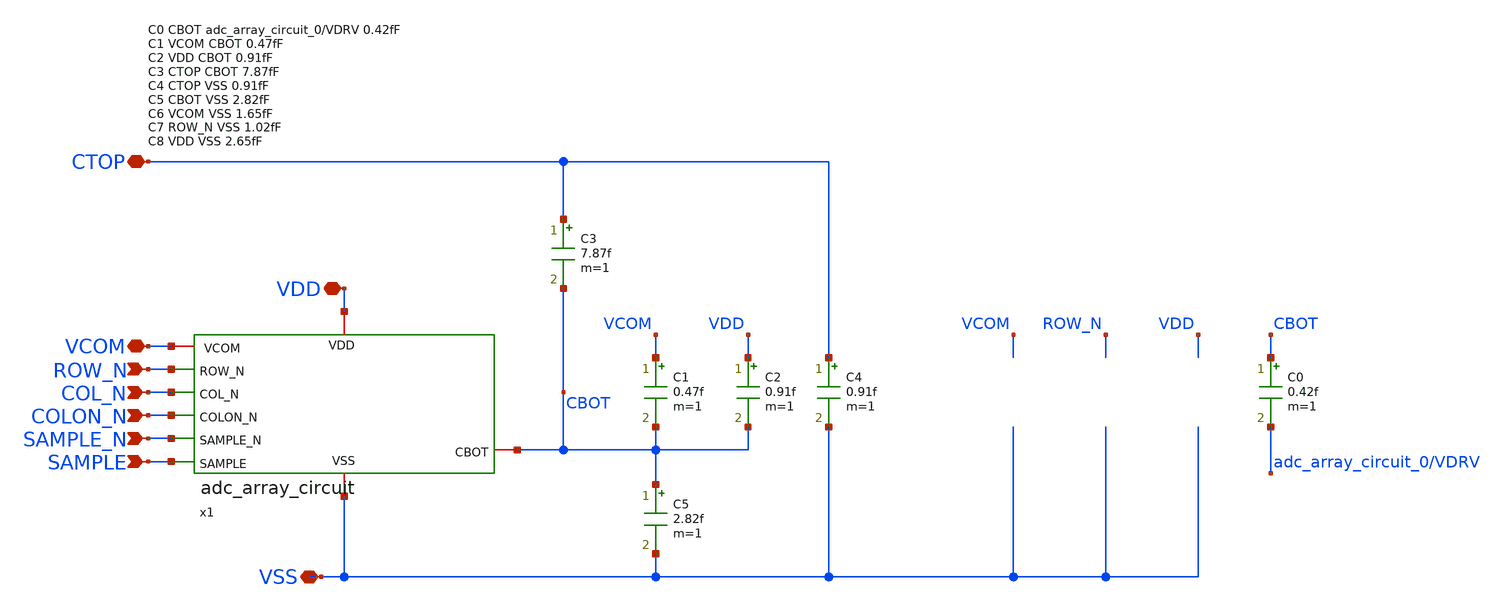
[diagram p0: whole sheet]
** sch_path: xschem/adc_array_cap/adc_array_cap_16.sch
**.subckt adc_array_cap_16 SAMPLE_N SAMPLE VCOM ROW_N COL_N COLON_N VDD CTOP VSS
*.ipin SAMPLE_N
*.ipin SAMPLE
*.iopin VCOM
*.ipin ROW_N
*.ipin COL_N
*.ipin COLON_N
*.iopin VDD
*.iopin CTOP
*.iopin VSS
C3 CTOP CBOT 7.87f m=1
C1 VCOM CBOT 0.47f m=1
C2 VDD CBOT 0.91f m=1
C4 CTOP VSS 0.91f m=1
C5 CBOT VSS 2.82f m=1
x1 VDD ROW_N CBOT COL_N COLON_N SAMPLE_N VCOM SAMPLE VSS adc_array_circuit
C0 CBOT adc_array_circuit_0/VDRV 0.42f m=1
**.ends

* expanding   symbol:  adc_array_circuit.sym # of pins=9
** sym_path: xschem/adc_array_cap/adc_array_circuit.sym
** sch_path: xschem/adc_array_cap/adc_array_circuit.sch
.subckt adc_array_circuit VDD ROW_N CBOT COL_N COLON_N SAMPLE_N VCOM SAMPLE VSS
*.ipin SAMPLE_N
*.ipin SAMPLE
*.iopin VCOM
*.ipin ROW_N
*.ipin COL_N
*.ipin COLON_N
*.iopin VDD
*.iopin VSS
*.iopin CBOT
XM1 VCOM SAMPLE CBOT VSS sky130_fd_pr__nfet_01v8 L=0.18 W=0.42 nf=1 ad='int((nf+1)/2) * W/nf * 0.29'
+ as='int((nf+2)/2) * W/nf * 0.29' pd='2*int((nf+1)/2) * (W/nf + 0.29)' ps='2*int((nf+2)/2) * (W/nf + 0.29)'
+ nrd='0.29 / W' nrs='0.29 / W' sa=0 sb=0 sd=0 mult=1 m=1
XM3 VCOM SAMPLE_N CBOT VDD sky130_fd_pr__pfet_01v8 L=0.18 W=0.9 nf=1 ad='int((nf+1)/2) * W/nf * 0.29'
+ as='int((nf+2)/2) * W/nf * 0.29' pd='2*int((nf+1)/2) * (W/nf + 0.29)' ps='2*int((nf+2)/2) * (W/nf + 0.29)'
+ nrd='0.29 / W' nrs='0.29 / W' sa=0 sb=0 sd=0 mult=1 m=1
XM2 VDRV SAMPLE_N CBOT VSS sky130_fd_pr__nfet_01v8 L=0.18 W=0.42 nf=1 ad='int((nf+1)/2) * W/nf * 0.29'
+ as='int((nf+2)/2) * W/nf * 0.29' pd='2*int((nf+1)/2) * (W/nf + 0.29)' ps='2*int((nf+2)/2) * (W/nf + 0.29)'
+ nrd='0.29 / W' nrs='0.29 / W' sa=0 sb=0 sd=0 mult=1 m=1
XM4 VDRV SAMPLE CBOT VDD sky130_fd_pr__pfet_01v8 L=0.18 W=0.9 nf=1 ad='int((nf+1)/2) * W/nf * 0.29' as='int((nf+2)/2) * W/nf * 0.29'
+ pd='2*int((nf+1)/2) * (W/nf + 0.29)' ps='2*int((nf+2)/2) * (W/nf + 0.29)' nrd='0.29 / W' nrs='0.29 / W'
+ sa=0 sb=0 sd=0 mult=1 m=1
XM5 VINT1 COL_N VDRV VDD sky130_fd_pr__pfet_01v8 L=0.18 W=0.9 nf=1 ad='int((nf+1)/2) * W/nf * 0.29' as='int((nf+2)/2) * W/nf * 0.29'
+ pd='2*int((nf+1)/2) * (W/nf + 0.29)' ps='2*int((nf+2)/2) * (W/nf + 0.29)' nrd='0.29 / W' nrs='0.29 / W'
+ sa=0 sb=0 sd=0 mult=1 m=1
XM6 VDD ROW_N VINT1 VDD sky130_fd_pr__pfet_01v8 L=0.18 W=0.9 nf=1 ad='int((nf+1)/2) * W/nf * 0.29' as='int((nf+2)/2) * W/nf * 0.29'
+ pd='2*int((nf+1)/2) * (W/nf + 0.29)' ps='2*int((nf+2)/2) * (W/nf + 0.29)' nrd='0.29 / W' nrs='0.29 / W'
+ sa=0 sb=0 sd=0 mult=1 m=1
XM7 VDD COLON_N VDRV VDD sky130_fd_pr__pfet_01v8 L=0.18 W=0.9 nf=1 ad='int((nf+1)/2) * W/nf * 0.29' as='int((nf+2)/2) * W/nf * 0.29'
+ pd='2*int((nf+1)/2) * (W/nf + 0.29)' ps='2*int((nf+2)/2) * (W/nf + 0.29)' nrd='0.29 / W' nrs='0.29 / W'
+ sa=0 sb=0 sd=0 mult=1 m=1
XM8 VINT2 COLON_N VDRV VSS sky130_fd_pr__nfet_01v8 L=0.18 W=0.42 nf=1 ad='int((nf+1)/2) * W/nf * 0.29'
+ as='int((nf+2)/2) * W/nf * 0.29' pd='2*int((nf+1)/2) * (W/nf + 0.29)' ps='2*int((nf+2)/2) * (W/nf + 0.29)'
+ nrd='0.29 / W' nrs='0.29 / W' sa=0 sb=0 sd=0 mult=1 m=1
XM9 VSS ROW_N VINT2 VSS sky130_fd_pr__nfet_01v8 L=0.18 W=0.42 nf=1 ad='int((nf+1)/2) * W/nf * 0.29' as='int((nf+2)/2) * W/nf * 0.29'
+ pd='2*int((nf+1)/2) * (W/nf + 0.29)' ps='2*int((nf+2)/2) * (W/nf + 0.29)' nrd='0.29 / W' nrs='0.29 / W'
+ sa=0 sb=0 sd=0 mult=1 m=1
XM10 VSS COL_N VINT2 VSS sky130_fd_pr__nfet_01v8 L=0.18 W=0.42 nf=1 ad='int((nf+1)/2) * W/nf * 0.29'
+ as='int((nf+2)/2) * W/nf * 0.29' pd='2*int((nf+1)/2) * (W/nf + 0.29)' ps='2*int((nf+2)/2) * (W/nf + 0.29)'
+ nrd='0.29 / W' nrs='0.29 / W' sa=0 sb=0 sd=0 mult=1 m=1
C0 COLON_N COL_N 1.23f m=1
C1 VDRV COL_N 0.98f m=1
C2 SAMPLE_N VDD 1.16f m=1
C VCOM VSS 1.65f m=1
C5 ROW_N VSS 1.02f m=1
C6 VDD VSS 2.65f m=1
C3 COLON_N SAMPLE 0.69f m=1
.ends

.end
